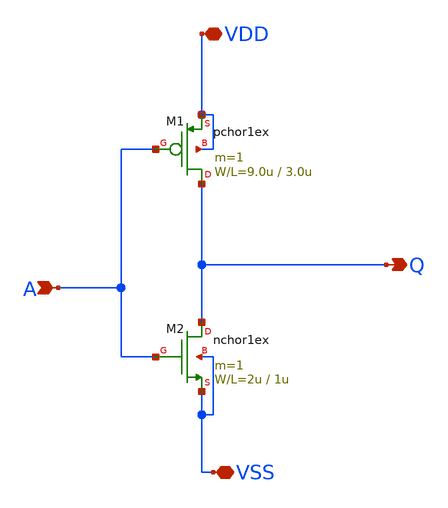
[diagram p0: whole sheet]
** sch_path: member_project/zakiryo1016/sr_inverter.sch
**.subckt sr_inverter A Q VSS VDD
*.ipin A
*.opin Q
*.iopin VSS
*.iopin VDD
M1 Q A VDD VDD pchor1ex L=3.0u W=9.0u m=1
M2 Q A VSS VSS nchor1ex L=1u W=2u m=1
**.ends
.end
